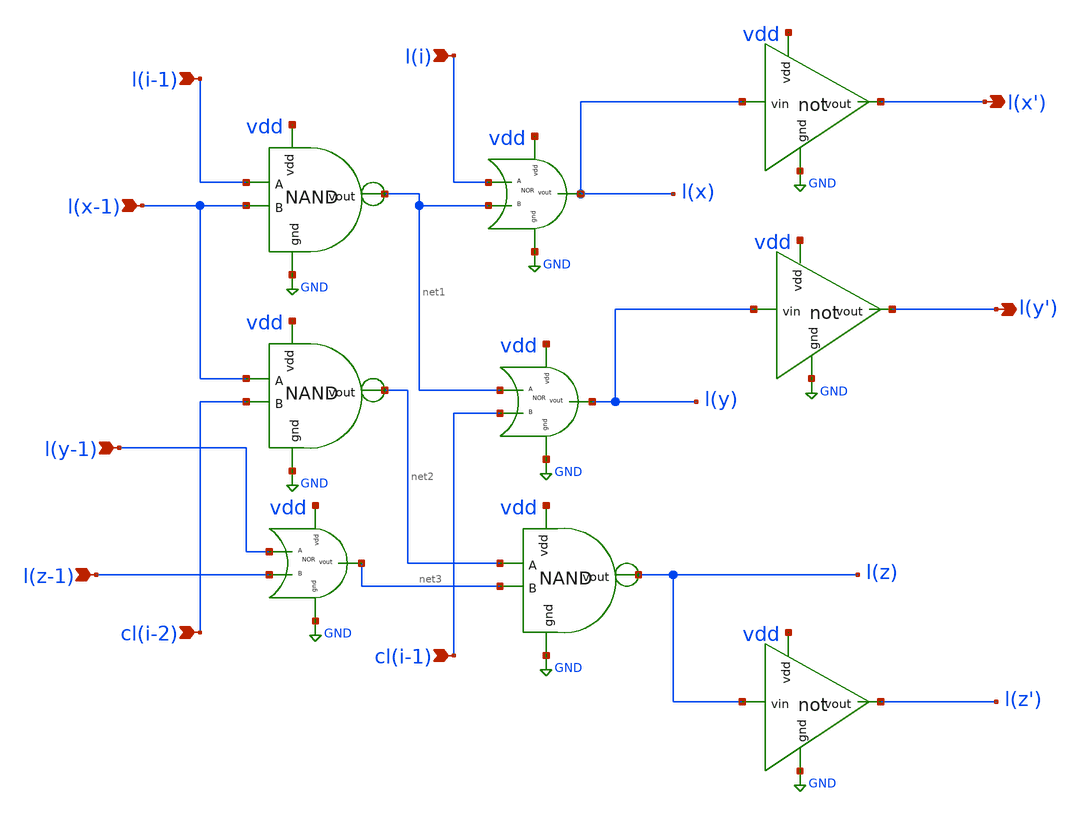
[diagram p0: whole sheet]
** sch_path: config_block.sch
**.subckt config_block l(i-1) l(i) l(x-1) cl(i-2) cl(i-1) l(y-1) l(z-1) l(y') l(x')
*.ipin l(i-1)
*.ipin l(i)
*.ipin l(x-1)
*.ipin cl(i-2)
*.ipin cl(i-1)
*.ipin l(y-1)
*.ipin l(z-1)
*.opin l(y')
*.opin l(x')
x1 vdd net2 GND l(x-1) cl(i-2) nand
x2 l(y) net1 cl(i-1) vdd GND nor
x4 vdd net1 GND l(i-1) l(x-1) nand
x5 net3 l(y-1) l(z-1) vdd GND nor
x6 l(x) l(i) net1 vdd GND nor
x7 vdd l(z) GND net2 net3 nand
x8 l(x') vdd GND l(x) not
x3 l(z') vdd GND l(z) not
x9 l(y') vdd GND l(y) not
**.ends
.GLOBAL GND
.end
